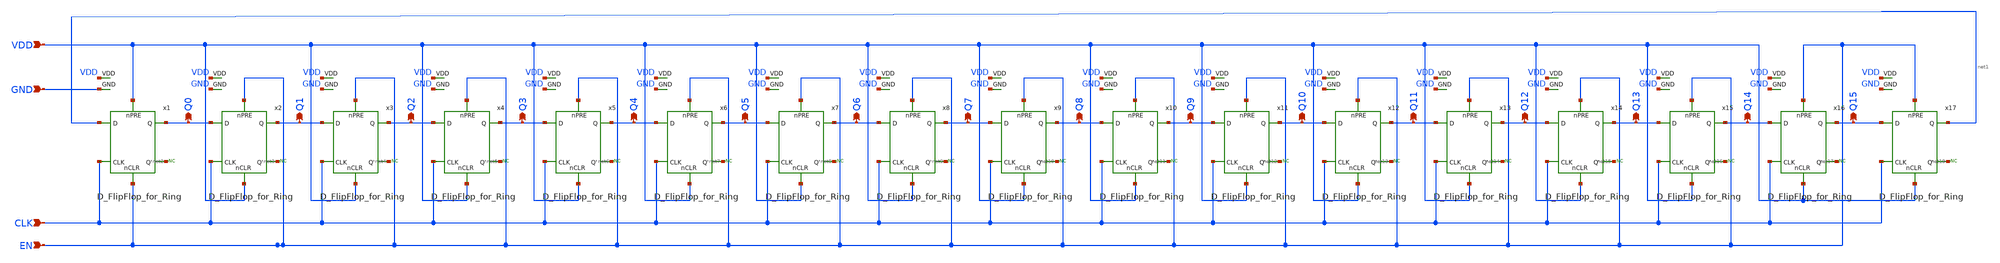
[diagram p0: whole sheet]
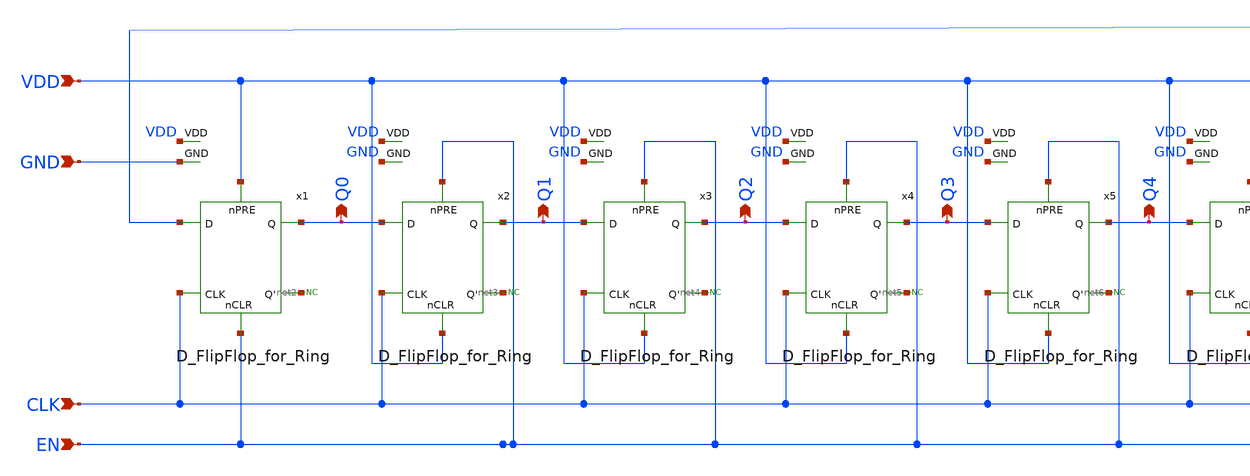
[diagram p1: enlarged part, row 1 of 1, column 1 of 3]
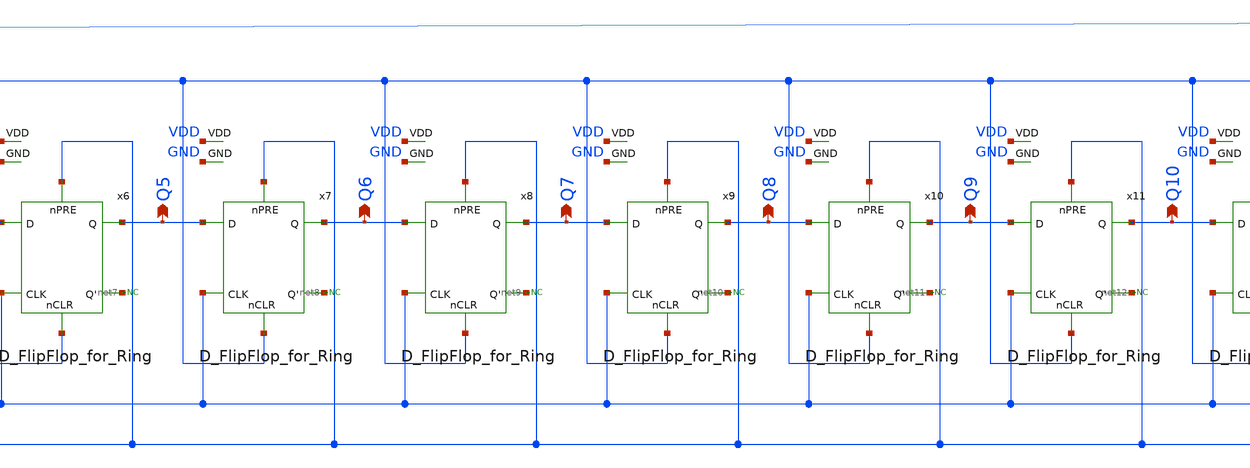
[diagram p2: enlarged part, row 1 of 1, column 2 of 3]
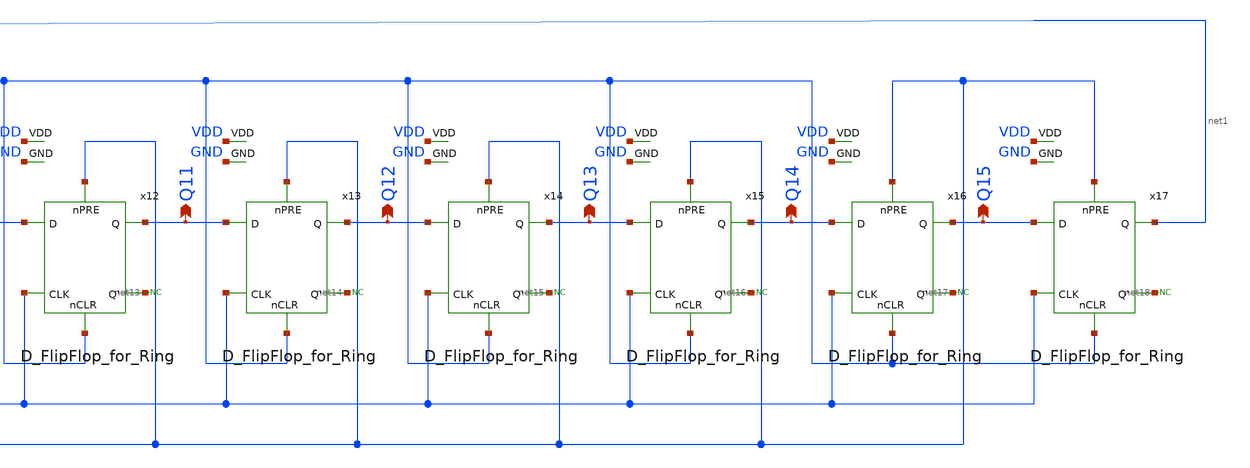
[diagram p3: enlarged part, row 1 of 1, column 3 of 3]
** sch_path: xschem/schematic_lvs/RING_COUNTER_FINAL.sch
**.subckt RING_COUNTER_FINAL Q0 Q1 Q2 Q3 Q4 Q5 Q6 Q7 Q8 Q9 Q10 Q11 Q12 Q13 Q14 Q15 CLK EN VDD GND
*.opin Q0
*.opin Q1
*.opin Q2
*.opin Q3
*.opin Q4
*.opin Q5
*.opin Q6
*.opin Q7
*.opin Q8
*.opin Q9
*.opin Q10
*.opin Q11
*.opin Q12
*.opin Q13
*.opin Q14
*.opin Q15
*.ipin CLK
*.ipin EN
*.ipin VDD
*.ipin GND
x1 VDD net1 Q0 CLK net2 EN GND VDD D_FlipFlop_for_Ring
x2 EN Q0 Q1 CLK net3 VDD GND VDD D_FlipFlop_for_Ring
x3 EN Q1 Q2 CLK net4 VDD GND VDD D_FlipFlop_for_Ring
x4 EN Q2 Q3 CLK net5 VDD GND VDD D_FlipFlop_for_Ring
x5 EN Q3 Q4 CLK net6 VDD GND VDD D_FlipFlop_for_Ring
x6 EN Q4 Q5 CLK net7 VDD GND VDD D_FlipFlop_for_Ring
x7 EN Q5 Q6 CLK net8 VDD GND VDD D_FlipFlop_for_Ring
x8 EN Q6 Q7 CLK net9 VDD GND VDD D_FlipFlop_for_Ring
x9 EN Q7 Q8 CLK net10 VDD GND VDD D_FlipFlop_for_Ring
x10 EN Q8 Q9 CLK net11 VDD GND VDD D_FlipFlop_for_Ring
x11 EN Q9 Q10 CLK net12 VDD GND VDD D_FlipFlop_for_Ring
x12 EN Q10 Q11 CLK net13 VDD GND VDD D_FlipFlop_for_Ring
x13 EN Q11 Q12 CLK net14 VDD GND VDD D_FlipFlop_for_Ring
x14 EN Q12 Q13 CLK net15 VDD GND VDD D_FlipFlop_for_Ring
x15 EN Q13 Q14 CLK net16 VDD GND VDD D_FlipFlop_for_Ring
x16 EN Q14 Q15 CLK net17 VDD GND VDD D_FlipFlop_for_Ring
x17 EN Q15 net1 CLK net18 VDD GND VDD D_FlipFlop_for_Ring
* noconn #net2
* noconn #net3
* noconn #net4
* noconn #net5
* noconn #net6
* noconn #net7
* noconn #net8
* noconn #net9
* noconn #net10
* noconn #net11
* noconn #net12
* noconn #net13
* noconn #net14
* noconn #net18
* noconn #net17
* noconn #net16
* noconn #net15
**.ends
.end
